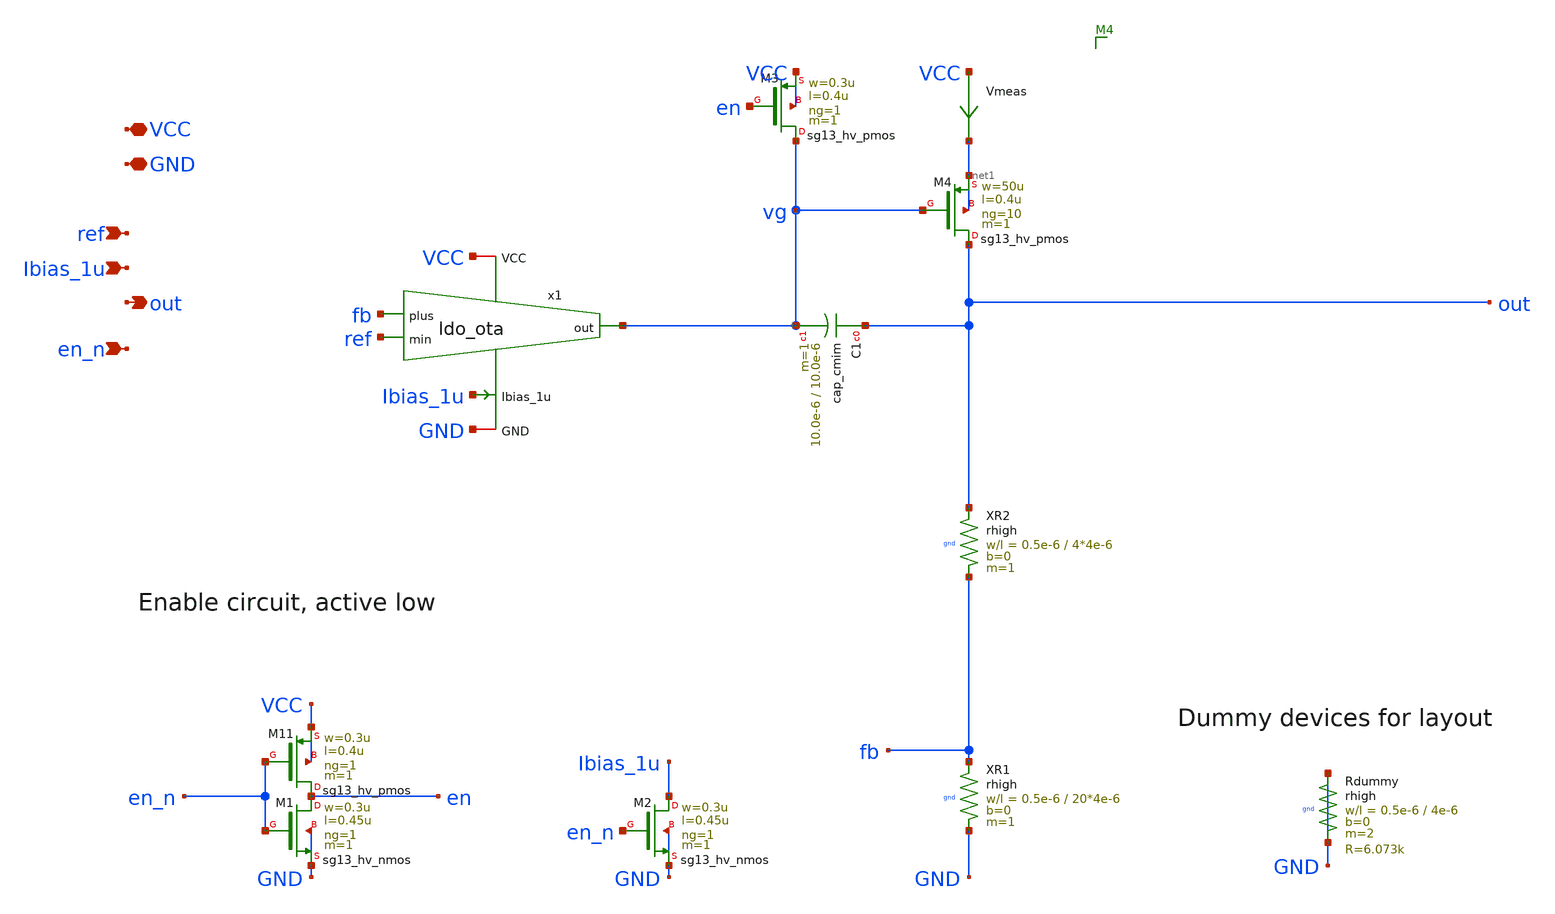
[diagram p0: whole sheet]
** sch_path: FLDO/design_data/xschem/ldo_1v2.sch
**.subckt ldo_1v2 VCC GND ref Ibias_1u out en_n
*.iopin VCC
*.iopin GND
*.ipin ref
*.ipin Ibias_1u
*.opin out
*.ipin en_n
XM4 out vg net1 net1 sg13_hv_pmos w=50u l=0.4u ng=10 m=1 mm_ok=1
Vmeas VCC net1 0
.save i(vmeas)
XC1 out vg cap_cmim w=10.0e-6 l=10.0e-6 m=1
XM2 Ibias_1u en_n GND GND sg13_hv_nmos w=0.3u l=0.45u ng=1 m=1 mm_ok=1
XM3 vg en VCC VCC sg13_hv_pmos w=0.3u l=0.4u ng=1 m=1 mm_ok=1
XM1 en en_n GND GND sg13_hv_nmos w=0.3u l=0.45u ng=1 m=1 mm_ok=1
XM11 en en_n VCC VCC sg13_hv_pmos w=0.3u l=0.4u ng=1 m=1 mm_ok=1
XRdummy GND GND gnd rhigh w=0.5e-6 l=4e-6 m=2 b=0 mm_ok=1
x1 VCC GND Ibias_1u fb ref vg ldo_ota
XR2 fb out gnd rhigh w=0.5e-6 l=4*4e-6 m=1 b=0
XR1 GND fb gnd rhigh w=0.5e-6 l=20*4e-6 m=1 b=0
**.ends

* expanding   symbol:  ldo_ota.sym # of pins=6
** sym_path: FLDO/design_data/xschem/ldo_ota.sym
** sch_path: FLDO/design_data/xschem/ldo_ota.sch
.subckt ldo_ota VCC GND Ibias_1u plus min out
*.iopin VCC
*.iopin GND
*.ipin plus
*.ipin min
*.opin out
*.ipin Ibias_1u
XM5 vbp plus tail GND sg13_hv_nmos w=3u l=2u ng=3 m=1 mm_ok=1
XM6 out min tail GND sg13_hv_nmos w=3u l=2u ng=3 m=1 mm_ok=1
XM7 tail Ibias_1u GND GND sg13_hv_nmos w=1u l=2u ng=1 m=2 mm_ok=1
XM8 Ibias_1u Ibias_1u GND GND sg13_hv_nmos w=1u l=2u ng=1 m=1 mm_ok=1
XM9 out vbp VCC VCC sg13_hv_pmos w=2u l=2u ng=2 m=1 mm_ok=1
XM10 vbp vbp VCC VCC sg13_hv_pmos w=2u l=2u ng=2 m=1 mm_ok=1
XMdummy0 GND Ibias_1u GND GND sg13_hv_nmos w=1u l=2u ng=1 m=2 mm_ok=1
XMdummy1 tail tail tail GND sg13_hv_nmos w=1u l=2u ng=1 m=4 mm_ok=1
XMdummyP VCC vbp VCC VCC sg13_hv_pmos w=1u l=2u ng=1 m=2 mm_ok=1
.ends

.end
